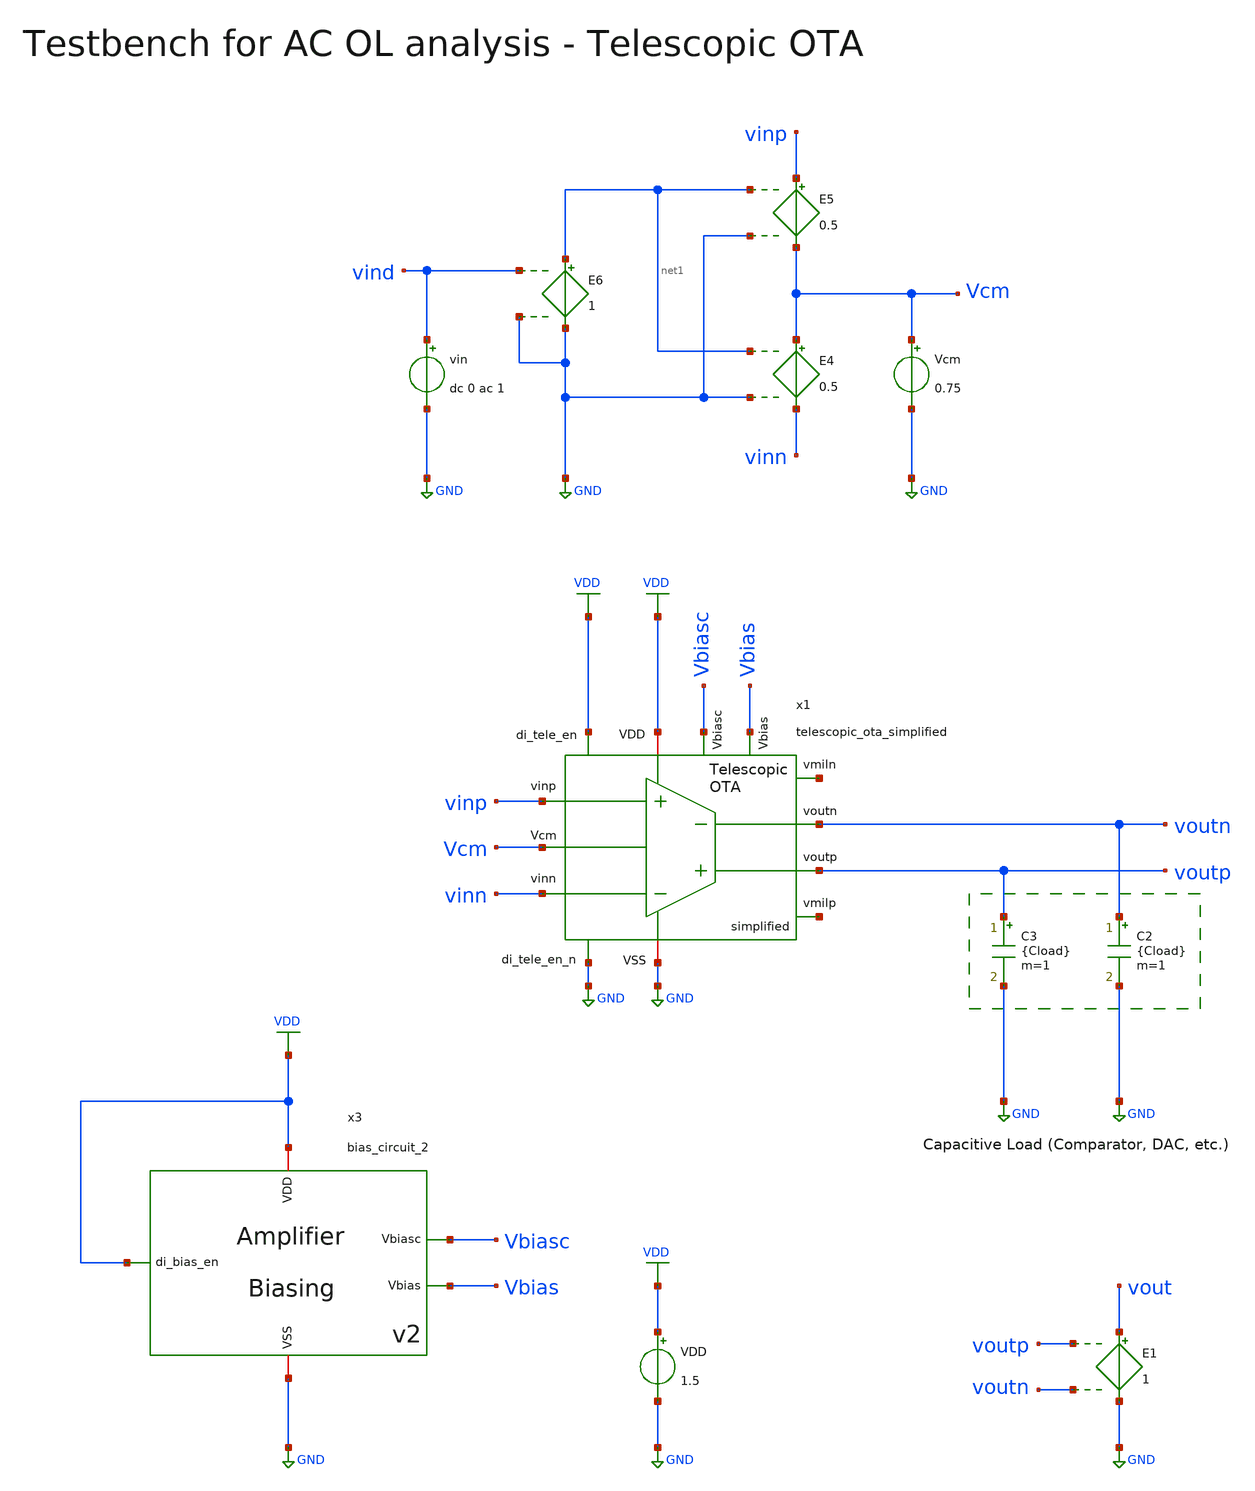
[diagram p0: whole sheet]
** sch_path: SG13G2_ATBS-ADC-main/xschem/bio_amplifier/amplifier_core/telescopic_ota/testbenches/telescopic_ota_simplified_tb_ac_ol.sch
**.subckt telescopic_ota_simplified_tb_ac_ol
VDD VDD GND 1.5
Vcm Vcm GND 0.75
E4 Vcm vinn net1 GND 0.5
E5 vinp Vcm net1 GND 0.5
E6 net1 GND vind GND 1
vin vind GND dc 0 ac 1
C2 voutn GND {Cload} m=1
C3 voutp GND {Cload} m=1
E1 vout GND voutp voutn 1
x1 net2 net3 voutp voutn VDD vinn vinp GND Vcm VDD GND Vbiasc Vbias telescopic_ota_simplified
x3 VDD Vbiasc VDD GND Vbias bias_circuit_2
**** begin user architecture code


.param temp=27
.param Cload=1p

.options savecurrents reltol=1e-3 abstol=1e-15 gmin=1e-15
.control
save all

set wr_vecnames
set wr_singlescale

* User Constants
let f_min = 0.01
let f_max = 1G
let fdc = 10

* Operating Point Analysis
op
remzerovec
write telescopic_ota_simplified_tb_ac_ol.raw
set appendwrite

* AC Analysis
ac dec 101 $&const.f_min $&const.f_max
remzerovec
write telescopic_ota_simplified_tb_ac_ol.raw

* Plotting
let Aol = v(vout)/v(vind)
let Aol_dB = vdb(Aol)
let Aol_arg = 180/PI*cphase(Aol)

plot Aol_dB ylabel 'Magnitude'
plot Aol_arg ylabel 'Phase'
plot Aol_dB Aol_arg ylabel 'Magnitude, Phase'

* Measurements
* DC open-loop gain
meas ac Adc_ol_dB find Aol_dB when frequency = fdc
print Adc_ol_dB

* 3dB cut-off frequency
let Aol_fc = Adc_ol_dB - 3
meas ac fc find frequency when Aol_dB = Aol_fc
print fc

* Unity Gain Bandwidth (Aol=1 or Aol_dB = 0dB)
meas ac UGB when Aol_dB=0  fall=1
print UGB

* Phase Margin at Aol=1 or Aol_dB = 0dB
meas ac arg_0dB find Aol_arg when Aol_dB=0
let PM = abs(arg_0dB)
print PM

* RHZ Frequency
meas ac Adc_ol_dB_min MIN Aol_dB
let Aol_fz = Adc_ol_dB_min + 3
meas ac fz find frequency when Aol_dB = Aol_fz
print fz

* Write Data
set wr_vecnames
set wr_singlescale
wrdata
+ /foss/designs/SG13G2_ATBS-ADC-main/python/plot_simulations/data/telescopic_ota_simplified_tb_ac_ol.txt v(Aol_dB) v(Aol_arg)

*quit
.endc



.lib cornerMOSlv.lib mos_tt
.lib cornerMOShv.lib mos_tt
.lib cornerRES.lib res_typ

**** end user architecture code
**.ends

* expanding   symbol:  bio_amplifier/amplifier_core/telescopic_ota/telescopic_ota_simplified.sym #
*+ of pins=13
** sym_path: SG13G2_ATBS-ADC-main/xschem/bio_amplifier/amplifier_core/telescopic_ota/telescopic_ota_simplified.sym
** sch_path: SG13G2_ATBS-ADC-main/xschem/bio_amplifier/amplifier_core/telescopic_ota/telescopic_ota_simplified.sch
.subckt telescopic_ota_simplified vmiln vmilp voutp voutn VDD vinn vinp VSS Vcm di_tele_en
+ di_tele_en_n Vbiasc Vbias
*.ipin vinp
*.ipin vinn
*.opin voutp
*.opin voutn
*.iopin VDD
*.iopin VSS
*.ipin Vcm
*.ipin di_tele_en
*.ipin di_tele_en_n
*.ipin vmilp
*.ipin vmiln
*.ipin Vbias
*.ipin Vbiasc
R1 net1 voutn 25.5Meg m=1
C1 net1 voutn 900f m=1
C2 voutp net1 900f m=1
R2 voutp net1 25.5Meg m=1
xM6 net3 Vgs_m56 VDD VDD sg13g2_lv_pmos_stacked_x2 W_P=1.0u L_P=20.0u NG_P=1 M_P=1
xM5 net2 Vgs_m56 VDD VDD sg13g2_lv_pmos_stacked_x2 W_P=8.0u L_P=20.0u NG_P=8 M_P=1
xM5c Vtail net10 net2 net2 sg13g2_lv_pmos_stacked_x2 W_P=8.0u L_P=20.0u NG_P=8 M_P=1
xM7 net7 net7 net6 net6 sg13g2_lv_pmos_stacked_x2 W_P=0.5u L_P=20.0u NG_P=1 M_P=1
XM1 vmiln vinp net4 net6 sg13_lv_pmos w=250.0u l=10.0u ng=250 m=1 mm_ok=1
XM1c voutn net7 vmiln vmiln sg13_lv_pmos w=15.0u l=10.0u ng=15 m=1 mm_ok=1
XM2c voutp net7 vmilp vmilp sg13_lv_pmos w=15.0u l=10.0u ng=15 m=1 mm_ok=1
XM2 vmilp vinn net5 net6 sg13_lv_pmos w=250.0u l=10.0u ng=250 m=1 mm_ok=1
xM3 voutn net1 VSS VSS sg13g2_lv_nmos_stacked_x4 W_N=1.5u L_N=40.0u NG_N=1 M_N=1
xM4 voutp net1 VSS VSS sg13g2_lv_nmos_stacked_x4 W_N=1.5u L_N=40.0u NG_N=1 M_N=1
Vmeas net9 net4 0
.save i(vmeas)
Vmeas1 net9 net5 0
.save i(vmeas1)
Vmeas2 net9 net6 0
.save i(vmeas2)
xM6c net8 net10 net3 net3 sg13g2_lv_pmos_stacked_x2 W_P=1.0u L_P=20.0u NG_P=1 M_P=1
XMpd4 Vcm di_tele_en_n net10 VDD sg13_hv_pmos w=1.0u l=0.5u ng=1 m=1 mm_ok=1
XMdec1 VDD Vgs_m56 VDD VDD sg13_lv_pmos w=10.0u l=40.0u ng=10 m=1 mm_ok=1
XMpd3 net10 di_tele_en VDD VDD sg13_hv_pmos w=1.0u l=0.5u ng=1 m=1 mm_ok=1
XMpd2 net8 di_tele_en_n Vgs_m56 VDD sg13_hv_pmos w=1.0u l=0.5u ng=1 m=1 mm_ok=1
XMpd1 Vgs_m56 di_tele_en VDD VDD sg13_hv_pmos w=1.0u l=0.5u ng=1 m=1 mm_ok=1
XMdec3 VDD net10 VDD VDD sg13_lv_pmos w=10.0u l=40.0u ng=10 m=1 mm_ok=1
Vmeas3 net8 net12 0
.save i(vmeas3)
Vmeas4 net7 net14 0
.save i(vmeas4)
xM8c net12 Vbiasc VSS net11 sg13g2_lv_nmos_stacked_x2 W_N=20.0u L_N=20.0u NG_N=20 M_N=1
xM8 net11 Vbias VSS VSS sg13g2_lv_nmos_stacked_x2 W_N=20.0u L_N=20.0u NG_N=20 M_N=1
xM9c net14 Vbiasc VSS net13 sg13g2_lv_nmos_stacked_x2 W_N=10.0u L_N=20.0u NG_N=10 M_N=1
xM9 net13 Vbias VSS VSS sg13g2_lv_nmos_stacked_x2 W_N=10.0u L_N=20.0u NG_N=10 M_N=1
Vmeas5 Vtail net9 0
.save i(vmeas5)
.ends


* expanding   symbol:  bio_amplifier/amplifier_core/bias_circuit/bias_circuit_2/bias_circuit_2.sym #
*+ of pins=5
** sym_path: SG13G2_ATBS-ADC-main/xschem/bio_amplifier/amplifier_core/bias_circuit/bias_circuit_2/bias_circuit_2.sym
** sch_path: SG13G2_ATBS-ADC-main/xschem/bio_amplifier/amplifier_core/bias_circuit/bias_circuit_2/bias_circuit_2.sch
.subckt bias_circuit_2 di_bias_en Vbiasc VDD VSS Vbias
*.iopin VDD
*.iopin VSS
*.opin Vbias
*.ipin di_bias_en
*.opin Vbiasc
R1 net3 VSS 3.72Meg m=1
XMDEC1 net1 Vbias net1 net1 sg13_lv_nmos w=100.0u l=40.0u ng=100 m=1 mm_ok=1
VIref net4 net8 0
.save i(viref)
VIout net9 Vbiasc 0
.save i(viout)
x1 VDD di_bias_en bias_en_n VSS inverter_lv W_P=1.0u L_P=0.13u W_N=1.0u L_N=0.13u
xMSU2 Vsu net6 VSS VSS sg13g2_lv_nmos_stacked_x4 W_N=1.0u L_N=40.0u NG_N=1 M_N=1
xMSU1 net5 Vsu VSS net6 sg13g2_lv_nmos_stacked_x4 W_N=1.0u L_N=40.0u NG_N=1 M_N=1
Vmeas1 net4 net5 0
.save i(vmeas1)
Vmeas2 Vbias net6 0
.save i(vmeas2)
XMPD1 Vgs_m34 di_bias_en net2 net2 sg13_lv_pmos w=1.0u l=0.13u ng=1 m=1 mm_ok=1
XMPD2 net4 bias_en_n Vgs_m34 net2 sg13_lv_pmos w=1.0u l=0.13u ng=1 m=1 mm_ok=1
XMPD3 Vbias bias_en_n VSS VSS sg13_lv_nmos w=1.0u l=0.13u ng=1 m=1 mm_ok=1
VIref5 net1 VSS 0
.save i(viref5)
VIdd VDD net2 0
.save i(vidd)
CSU1 net10 Vsu 35f m=1
xM1 net7 Vbias VSS net3 sg13g2_lv_nmos_stacked_x2 W_N=20.0u L_N=20.0u NG_N=20 M_N=1
xM1c net8 Vbiasc VSS net7 sg13g2_lv_nmos_stacked_x2 W_N=5.0u L_N=20.0u NG_N=5 M_N=1
xM2 Vbias Vbias VSS VSS sg13g2_lv_nmos_stacked_x2 W_N=5.0u L_N=20.0u NG_N=5 M_N=1
xM2c Vbiasc Vbiasc VSS Vbias sg13g2_lv_nmos_stacked_x2 W_N=5.0u L_N=20.0u NG_N=5 M_N=1
XMDEC2 net2 Vgs_m34 net2 net2 sg13_lv_pmos w=25.0u l=40.0u ng=25 m=1 mm_ok=1
xM3 net4 Vgs_m34 net2 net2 sg13g2_lv_pmos_stacked_x4 W_P=20.0u L_P=40.0u NG_P=20 M_P=1
xM4 net9 Vgs_m34 net2 net2 sg13g2_lv_pmos_stacked_x4 W_P=20.0u L_P=40.0u NG_P=20 M_P=1
XMPD6 Vsu di_bias_en net10 net10 sg13_lv_pmos w=1.0u l=0.13u ng=1 m=1 mm_ok=1
XMPD4 Vbiasc bias_en_n VSS VSS sg13_lv_nmos w=1.0u l=0.13u ng=1 m=1 mm_ok=1
XMPD7 Vsu bias_en_n VSS VSS sg13_lv_nmos w=1.0u l=0.13u ng=1 m=1 mm_ok=1
XMPD5 net10 bias_en_n net2 net2 sg13_lv_pmos w=1.0u l=0.13u ng=1 m=1 mm_ok=1
.ends


* expanding   symbol:  stacked_transistors/sg13g2_lv_pmos_stacked/sg13g2_lv_pmos_stacked_x2.sym # of
*+ pins=4
** sym_path: SG13G2_ATBS-ADC-main/xschem/stacked_transistors/sg13g2_lv_pmos_stacked/sg13g2_lv_pmos_stacked_x2.sym
** sch_path: SG13G2_ATBS-ADC-main/xschem/stacked_transistors/sg13g2_lv_pmos_stacked/sg13g2_lv_pmos_stacked_x2.sch
.subckt sg13g2_lv_pmos_stacked_x2 D G B S  W_P=1.0u L_P=0.45u NG_P=1 M_P=1
*.iopin D
*.iopin S
*.iopin G
*.iopin B
XM1 net1 G S B sg13_lv_pmos w=W_P l=L_P/2 ng=NG_P m=M_P mm_ok=1
XM2 D G net1 B sg13_lv_pmos w=W_P l=L_P/2 ng=NG_P m=M_P mm_ok=1
.ends


* expanding   symbol:  stacked_transistors/sg13g2_lv_nmos_stacked/sg13g2_lv_nmos_stacked_x4.sym # of
*+ pins=4
** sym_path: SG13G2_ATBS-ADC-main/xschem/stacked_transistors/sg13g2_lv_nmos_stacked/sg13g2_lv_nmos_stacked_x4.sym
** sch_path: SG13G2_ATBS-ADC-main/xschem/stacked_transistors/sg13g2_lv_nmos_stacked/sg13g2_lv_nmos_stacked_x4.sch
.subckt sg13g2_lv_nmos_stacked_x4 D G B S  W_N=1.0u L_N=0.45u NG_N=1 M_N=1
*.iopin D
*.iopin S
*.iopin G
*.iopin B
XM1 net1 G S B sg13_lv_nmos w=W_N l=L_N/4 ng=NG_N m=M_N mm_ok=1
XM2 net3 G net1 B sg13_lv_nmos w=W_N l=L_N/4 ng=NG_N m=M_N mm_ok=1
XM3 net2 G net3 B sg13_lv_nmos w=W_N l=L_N/4 ng=NG_N m=M_N mm_ok=1
XM4 D G net2 B sg13_lv_nmos w=W_N l=L_N/4 ng=NG_N m=M_N mm_ok=1
.ends


* expanding   symbol:  stacked_transistors/sg13g2_lv_nmos_stacked/sg13g2_lv_nmos_stacked_x2.sym # of
*+ pins=4
** sym_path: SG13G2_ATBS-ADC-main/xschem/stacked_transistors/sg13g2_lv_nmos_stacked/sg13g2_lv_nmos_stacked_x2.sym
** sch_path: SG13G2_ATBS-ADC-main/xschem/stacked_transistors/sg13g2_lv_nmos_stacked/sg13g2_lv_nmos_stacked_x2.sch
.subckt sg13g2_lv_nmos_stacked_x2 D G B S  W_N=1.0u L_N=0.45u NG_N=1 M_N=1
*.iopin D
*.iopin S
*.iopin G
*.iopin B
XM1 net1 G S B sg13_lv_nmos w=W_N l=L_N/2 ng=NG_N m=M_N mm_ok=1
XM2 D G net1 B sg13_lv_nmos w=W_N l=L_N/2 ng=NG_N m=M_N mm_ok=1
.ends


* expanding   symbol:  inverter/inverter_lv.sym # of pins=4
** sym_path: SG13G2_ATBS-ADC-main/xschem/inverter/inverter_lv.sym
** sch_path: SG13G2_ATBS-ADC-main/xschem/inverter/inverter_lv.sch
.subckt inverter_lv VDD vin vout VSS  W_P=3.0u L_P=0.13u W_N=1.0u L_N=0.13u
*.ipin vin
*.iopin VDD
*.iopin VSS
*.opin vout
XM1 vout vin VDD VDD sg13_lv_pmos w=W_P l=L_P ng=1 m=1 mm_ok=1
XM2 vout vin VSS VSS sg13_lv_nmos w=W_N l=L_N ng=1 m=1 mm_ok=1
.ends


* expanding   symbol:  stacked_transistors/sg13g2_lv_pmos_stacked/sg13g2_lv_pmos_stacked_x4.sym # of
*+ pins=4
** sym_path: SG13G2_ATBS-ADC-main/xschem/stacked_transistors/sg13g2_lv_pmos_stacked/sg13g2_lv_pmos_stacked_x4.sym
** sch_path: SG13G2_ATBS-ADC-main/xschem/stacked_transistors/sg13g2_lv_pmos_stacked/sg13g2_lv_pmos_stacked_x4.sch
.subckt sg13g2_lv_pmos_stacked_x4 D G B S  W_P=1.0u L_P=0.45u NG_P=1 M_P=1
*.iopin D
*.iopin S
*.iopin G
*.iopin B
XM1 net1 G S B sg13_lv_pmos w=W_P l=L_P/4 ng=NG_P m=M_P mm_ok=1
XM2 net3 G net1 B sg13_lv_pmos w=W_P l=L_P/4 ng=NG_P m=M_P mm_ok=1
XM3 net2 G net3 B sg13_lv_pmos w=W_P l=L_P/4 ng=NG_P m=M_P mm_ok=1
XM4 D G net2 B sg13_lv_pmos w=W_P l=L_P/4 ng=NG_P m=M_P mm_ok=1
.ends

.GLOBAL GND
.GLOBAL VDD
.end
